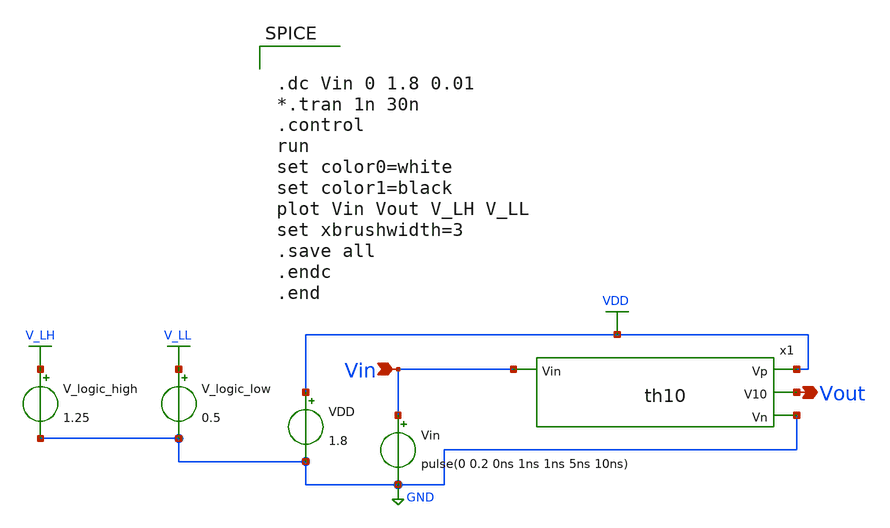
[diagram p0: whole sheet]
** sch_path: xschem/Vth_sch/Pre_layout/th10.sch
**.subckt th10 Vin Vout
*.ipin Vin
*.opin Vout
VDD VDD GND 1.8
Vin Vin GND pulse(0 0.2 0ns 1ns 1ns 5ns 10ns)
V_logic_high V_LH GND 1.25
V_logic_low V_LL GND 0.5
x1 VDD Vout Vin GND th10
**** begin user architecture code


.lib /usr/local/share/pdk/sky130A/libs.tech/ngspice/sky130.lib.spice tt

.save all





.dc Vin 0 1.8 0.01
*.tran 1n 30n
.control
run
set color0=white
set color1=black
plot Vin Vout V_LH V_LL
set xbrushwidth=3
.save all
.endc
.end


**** end user architecture code
**.ends

* expanding   symbol:  /home/exotic/Desktop/ASIC_ADC/xschem/Vth_sch/Symbol/th10.sym # of pins=4
** sym_path: xschem/Vth_sch/Symbol/th10.sym
** sch_path: xschem/Vth_sch/Symbol/th10.sch
.subckt th10 Vp V10 Vin Vn
*.opin Vn
*.opin Vp
*.ipin Vin
*.opin V10
XM3 V10 net1 Vp Vp sky130_fd_pr__pfet_01v8 L=0.15 W=0.42 nf=1 ad='int((nf+1)/2) * W/nf * 0.29' as='int((nf+2)/2) * W/nf * 0.29'
+ pd='2*int((nf+1)/2) * (W/nf + 0.29)' ps='2*int((nf+2)/2) * (W/nf + 0.29)' nrd='0.29 / W' nrs='0.29 / W'
+ sa=0 sb=0 sd=0 mult=1 m=1
XM4 V10 net1 Vn Vn sky130_fd_pr__nfet_01v8 L=0.18 W=0.42 nf=1 ad='int((nf+1)/2) * W/nf * 0.29' as='int((nf+2)/2) * W/nf * 0.29'
+ pd='2*int((nf+1)/2) * (W/nf + 0.29)' ps='2*int((nf+2)/2) * (W/nf + 0.29)' nrd='0.29 / W' nrs='0.29 / W'
+ sa=0 sb=0 sd=0 mult=1 m=1
XM2 net1 Vin Vp Vp sky130_fd_pr__pfet_01v8 L=0.28 W=0.42 nf=1 ad='int((nf+1)/2) * W/nf * 0.29' as='int((nf+2)/2) * W/nf * 0.29'
+ pd='2*int((nf+1)/2) * (W/nf + 0.29)' ps='2*int((nf+2)/2) * (W/nf + 0.29)' nrd='0.29 / W' nrs='0.29 / W'
+ sa=0 sb=0 sd=0 mult=1 m=1
XM1 net1 Vin net2 Vn sky130_fd_pr__nfet_01v8 L=0.46 W=0.40 nf=1 ad='int((nf+1)/2) * W/nf * 0.29' as='int((nf+2)/2) * W/nf * 0.29'
+ pd='2*int((nf+1)/2) * (W/nf + 0.29)' ps='2*int((nf+2)/2) * (W/nf + 0.29)' nrd='0.29 / W' nrs='0.29 / W'
+ sa=0 sb=0 sd=0 mult=1 m=1
XM0 Vn Vn net2 Vp sky130_fd_pr__pfet_01v8 L=0.15 W=1 nf=1 ad='int((nf+1)/2) * W/nf * 0.29' as='int((nf+2)/2) * W/nf * 0.29'
+ pd='2*int((nf+1)/2) * (W/nf + 0.29)' ps='2*int((nf+2)/2) * (W/nf + 0.29)' nrd='0.29 / W' nrs='0.29 / W'
+ sa=0 sb=0 sd=0 mult=1 m=1
.ends

.GLOBAL VDD
.GLOBAL GND
.GLOBAL V_LH
.GLOBAL V_LL
.end
